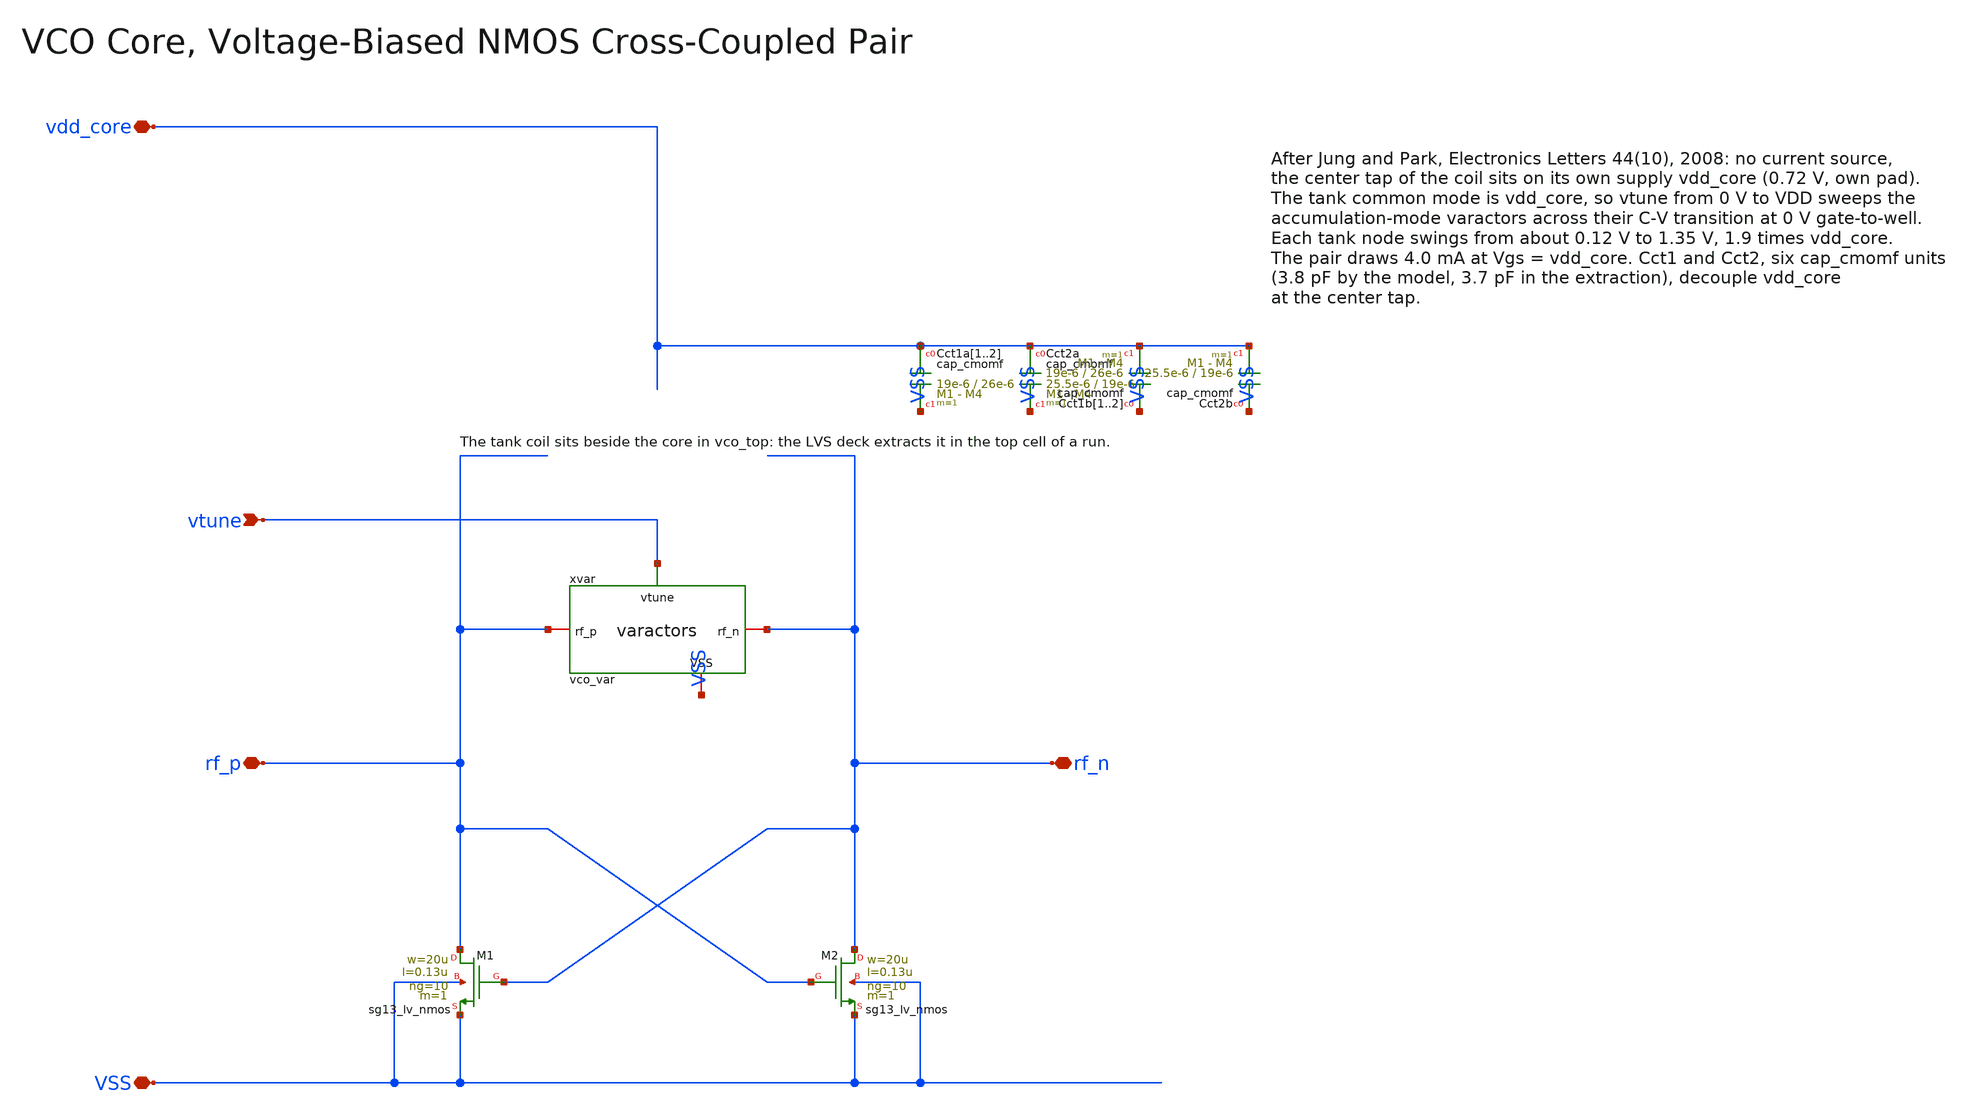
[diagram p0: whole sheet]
** sch_path: macros/vco/schematic/xschem/vco_core.sch
**.subckt vco_core vdd_core VSS vtune rf_p rf_n
*.iopin vdd_core
*.iopin VSS
*.ipin vtune
*.iopin rf_p
*.iopin rf_n
XCct1a1 vdd_core VSS cap_cmomf w=19e-6 l=26e-6 mmin=1 mmax=4 subblock=0 rfmodel=0 subscale=1 m=1
+ mm_ok=1
XCct1a2 vdd_core VSS cap_cmomf w=19e-6 l=26e-6 mmin=1 mmax=4 subblock=0 rfmodel=0 subscale=1 m=1
+ mm_ok=1
xvar rf_p rf_n vtune VSS vco_var
XM1 rf_p rf_n VSS VSS sg13_lv_nmos w=20u l=0.13u ng=10 m=1 mm_ok=1
XM2 rf_n rf_p VSS VSS sg13_lv_nmos w=20u l=0.13u ng=10 m=1 mm_ok=1
XCct2a vdd_core VSS cap_cmomf w=25.5e-6 l=19e-6 mmin=1 mmax=4 subblock=0 rfmodel=0 subscale=1 m=1
+ mm_ok=1
XCct1b1 VSS vdd_core cap_cmomf w=19e-6 l=26e-6 mmin=1 mmax=4 subblock=0 rfmodel=0 subscale=1 m=1
+ mm_ok=1
XCct1b2 VSS vdd_core cap_cmomf w=19e-6 l=26e-6 mmin=1 mmax=4 subblock=0 rfmodel=0 subscale=1 m=1
+ mm_ok=1
XCct2b VSS vdd_core cap_cmomf w=25.5e-6 l=19e-6 mmin=1 mmax=4 subblock=0 rfmodel=0 subscale=1 m=1
+ mm_ok=1
**.ends

* expanding   symbol:  vco_var.sym # of pins=4
** sym_path: vco_var.sym
** sch_path: vco_var.sch
.subckt vco_var rf_p rf_n vtune VSS
*.ipin vtune
*.iopin rf_p
*.iopin rf_n
*.iopin VSS
XCvar1 rf_p vtune rf_n VSS sg13_hv_svaricap w=3.74u l=0.3u Nx=8 mm_ok=1
XCvar2 rf_p vtune rf_n VSS sg13_hv_svaricap w=3.74u l=0.3u Nx=8 mm_ok=1
XCvar3 rf_p vtune rf_n VSS sg13_hv_svaricap w=3.74u l=0.3u Nx=8 mm_ok=1
.ends

.end
